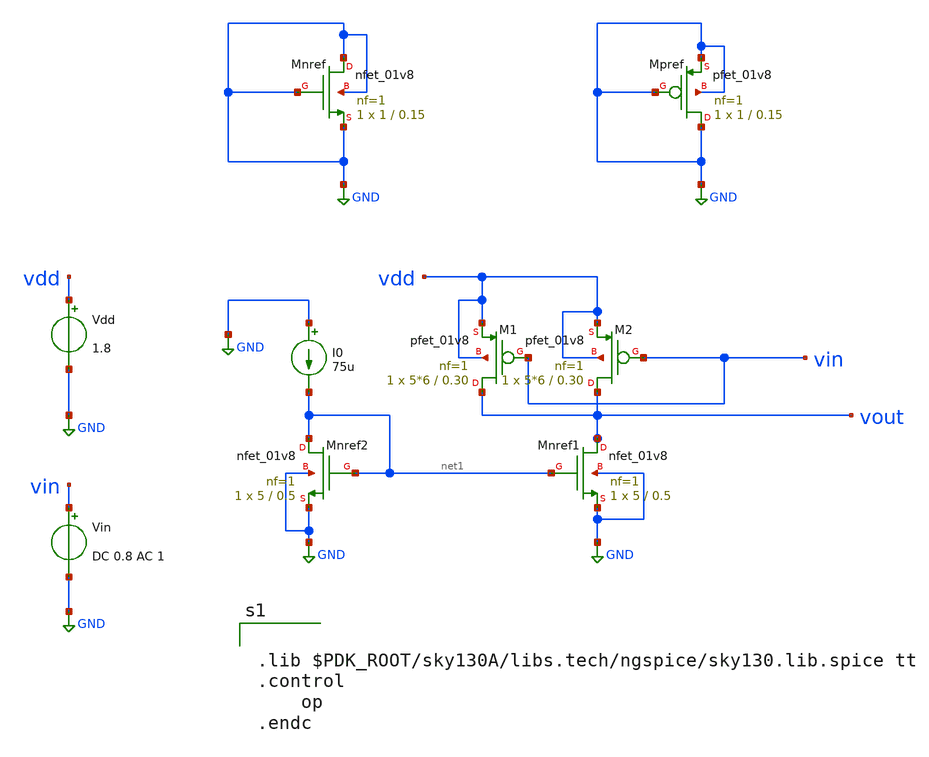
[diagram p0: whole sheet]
** sch_path: main.sch
**.subckt main
XMnref GND GND GND GND sky130_fd_pr__nfet_01v8 L=0.15 W=1 nf=1 ad='int((nf+1)/2) * W/nf * 0.29' as='int((nf+2)/2) * W/nf * 0.29'
+ pd='2*int((nf+1)/2) * (W/nf + 0.29)' ps='2*int((nf+2)/2) * (W/nf + 0.29)' nrd='0.29 / W' nrs='0.29 / W'
+ sa=0 sb=0 sd=0 mult=1 m=1
XMpref GND GND GND GND sky130_fd_pr__pfet_01v8 L=0.15 W=1 nf=1 ad='int((nf+1)/2) * W/nf * 0.29' as='int((nf+2)/2) * W/nf * 0.29'
+ pd='2*int((nf+1)/2) * (W/nf + 0.29)' ps='2*int((nf+2)/2) * (W/nf + 0.29)' nrd='0.29 / W' nrs='0.29 / W'
+ sa=0 sb=0 sd=0 mult=1 m=1
Vdd vdd GND 1.8
Vin vin GND DC 0.8 AC 1
XM2 vout vin vdd vdd sky130_fd_pr__pfet_01v8 L=0.30 W=5*6 nf=1 ad='int((nf+1)/2) * W/nf * 0.29' as='int((nf+2)/2) * W/nf * 0.29'
+ pd='2*int((nf+1)/2) * (W/nf + 0.29)' ps='2*int((nf+2)/2) * (W/nf + 0.29)' nrd='0.29 / W' nrs='0.29 / W'
+ sa=0 sb=0 sd=0 mult=1 m=1
XMnref1 vout net1 GND GND sky130_fd_pr__nfet_01v8 L=0.5 W=5 nf=1 ad='int((nf+1)/2) * W/nf * 0.29' as='int((nf+2)/2) * W/nf * 0.29'
+ pd='2*int((nf+1)/2) * (W/nf + 0.29)' ps='2*int((nf+2)/2) * (W/nf + 0.29)' nrd='0.29 / W' nrs='0.29 / W'
+ sa=0 sb=0 sd=0 mult=1 m=1
XMnref2 net1 net1 GND GND sky130_fd_pr__nfet_01v8 L=0.5 W=5 nf=1 ad='int((nf+1)/2) * W/nf * 0.29' as='int((nf+2)/2) * W/nf * 0.29'
+ pd='2*int((nf+1)/2) * (W/nf + 0.29)' ps='2*int((nf+2)/2) * (W/nf + 0.29)' nrd='0.29 / W' nrs='0.29 / W'
+ sa=0 sb=0 sd=0 mult=1 m=1
I0 GND net1 75u
XM1 vout vin vdd vdd sky130_fd_pr__pfet_01v8 L=0.30 W=5*6 nf=1 ad='int((nf+1)/2) * W/nf * 0.29' as='int((nf+2)/2) * W/nf * 0.29'
+ pd='2*int((nf+1)/2) * (W/nf + 0.29)' ps='2*int((nf+2)/2) * (W/nf + 0.29)' nrd='0.29 / W' nrs='0.29 / W'
+ sa=0 sb=0 sd=0 mult=1 m=1
**** begin user architecture code


.lib $PDK_ROOT/sky130A/libs.tech/ngspice/sky130.lib.spice tt
.control
    op
.endc


**** end user architecture code
**.ends
.GLOBAL GND
.end
